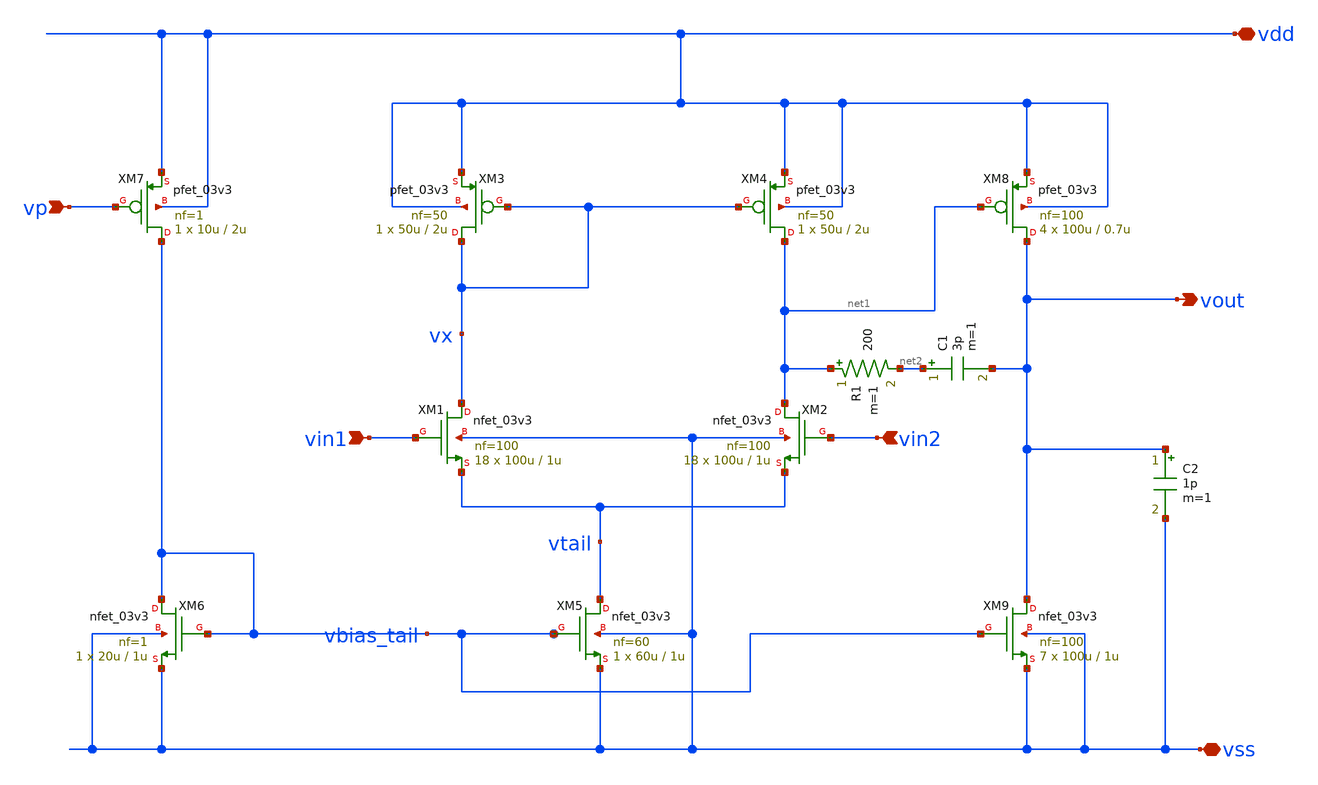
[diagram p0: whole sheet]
** sch_path: OTA_2stage.sch
**.subckt OTA_2stage vdd vss vin1 vin2 vp vout
*.iopin vdd
*.iopin vss
*.ipin vin1
*.ipin vin2
*.ipin vp
*.opin vout
XM1 vx vin1 vtail vss nfet_03v3 L=1u W=100u nf=100 ad='int((nf+1)/2) * W/nf * 0.18u' as='int((nf+2)/2) * W/nf * 0.18u'
+ pd='2*int((nf+1)/2) * (W/nf + 0.18u)' ps='2*int((nf+2)/2) * (W/nf + 0.18u)' nrd='0.18u / W' nrs='0.18u / W'
+ sa=0 sb=0 sd=0 m=18
XM2 net1 vin2 vtail vss nfet_03v3 L=1u W=100u nf=100 ad='int((nf+1)/2) * W/nf * 0.18u' as='int((nf+2)/2) * W/nf * 0.18u'
+ pd='2*int((nf+1)/2) * (W/nf + 0.18u)' ps='2*int((nf+2)/2) * (W/nf + 0.18u)' nrd='0.18u / W' nrs='0.18u / W'
+ sa=0 sb=0 sd=0 m=18
XM3 vx vx vdd vdd pfet_03v3 L=2u W=50u nf=50 ad='int((nf+1)/2) * W/nf * 0.18u' as='int((nf+2)/2) * W/nf * 0.18u'
+ pd='2*int((nf+1)/2) * (W/nf + 0.18u)' ps='2*int((nf+2)/2) * (W/nf + 0.18u)' nrd='0.18u / W' nrs='0.18u / W'
+ sa=0 sb=0 sd=0 m=1
XM4 net1 vx vdd vdd pfet_03v3 L=2u W=50u nf=50 ad='int((nf+1)/2) * W/nf * 0.18u' as='int((nf+2)/2) * W/nf * 0.18u'
+ pd='2*int((nf+1)/2) * (W/nf + 0.18u)' ps='2*int((nf+2)/2) * (W/nf + 0.18u)' nrd='0.18u / W' nrs='0.18u / W'
+ sa=0 sb=0 sd=0 m=1
XM5 vtail vbias_tail vss vss nfet_03v3 L=1u W=60u nf=60 ad='int((nf+1)/2) * W/nf * 0.18u' as='int((nf+2)/2) * W/nf * 0.18u'
+ pd='2*int((nf+1)/2) * (W/nf + 0.18u)' ps='2*int((nf+2)/2) * (W/nf + 0.18u)' nrd='0.18u / W' nrs='0.18u / W'
+ sa=0 sb=0 sd=0 m=1
XM6 vbias_tail vbias_tail vss vss nfet_03v3 L=1u W=20u nf=1 ad='int((nf+1)/2) * W/nf * 0.18u' as='int((nf+2)/2) * W/nf * 0.18u'
+ pd='2*int((nf+1)/2) * (W/nf + 0.18u)' ps='2*int((nf+2)/2) * (W/nf + 0.18u)' nrd='0.18u / W' nrs='0.18u / W'
+ sa=0 sb=0 sd=0 m=1
XM7 vbias_tail vp vdd vdd pfet_03v3 L=2u W=10u nf=1 ad='int((nf+1)/2) * W/nf * 0.18u' as='int((nf+2)/2) * W/nf * 0.18u'
+ pd='2*int((nf+1)/2) * (W/nf + 0.18u)' ps='2*int((nf+2)/2) * (W/nf + 0.18u)' nrd='0.18u / W' nrs='0.18u / W'
+ sa=0 sb=0 sd=0 m=1
XM8 vout net1 vdd vdd pfet_03v3 L=0.7u W=100u nf=100 ad='int((nf+1)/2) * W/nf * 0.18u' as='int((nf+2)/2) * W/nf * 0.18u'
+ pd='2*int((nf+1)/2) * (W/nf + 0.18u)' ps='2*int((nf+2)/2) * (W/nf + 0.18u)' nrd='0.18u / W' nrs='0.18u / W'
+ sa=0 sb=0 sd=0 m=4
XM9 vout vbias_tail vss vss nfet_03v3 L=1u W=100u nf=100 ad='int((nf+1)/2) * W/nf * 0.18u' as='int((nf+2)/2) * W/nf * 0.18u'
+ pd='2*int((nf+1)/2) * (W/nf + 0.18u)' ps='2*int((nf+2)/2) * (W/nf + 0.18u)' nrd='0.18u / W' nrs='0.18u / W'
+ sa=0 sb=0 sd=0 m=7
C2 vout vss 1p m=1
C1 net2 vout 3p m=1
R1 net1 net2 200 m=1
**.ends
.end
